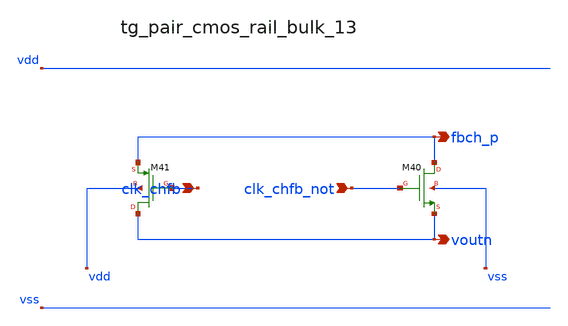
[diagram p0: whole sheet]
** sch_path: analog-db/raw/ia_003_fan_chopper_pf/hier/blocks/tg_pair_cmos_rail_bulk_13.sch
**.subckt tg_pair_cmos_rail_bulk_13 clk_chfb clk_chfb_not fbch_p voutn
*.ipin clk_chfb
*.ipin clk_chfb_not
*.opin fbch_p
*.opin voutn
XM40 fbch_p clk_chfb_not voutn vss sg13_lv_nmos w=x_dut_xm40_w l=x_dut_xm40_l ng=1 m=x_dut_xm40_m
XM41 voutn clk_chfb fbch_p vdd sg13_lv_pmos w=x_dut_xm41_w l=x_dut_xm41_l ng=1 m=x_dut_xm41_m
**.ends
.end
